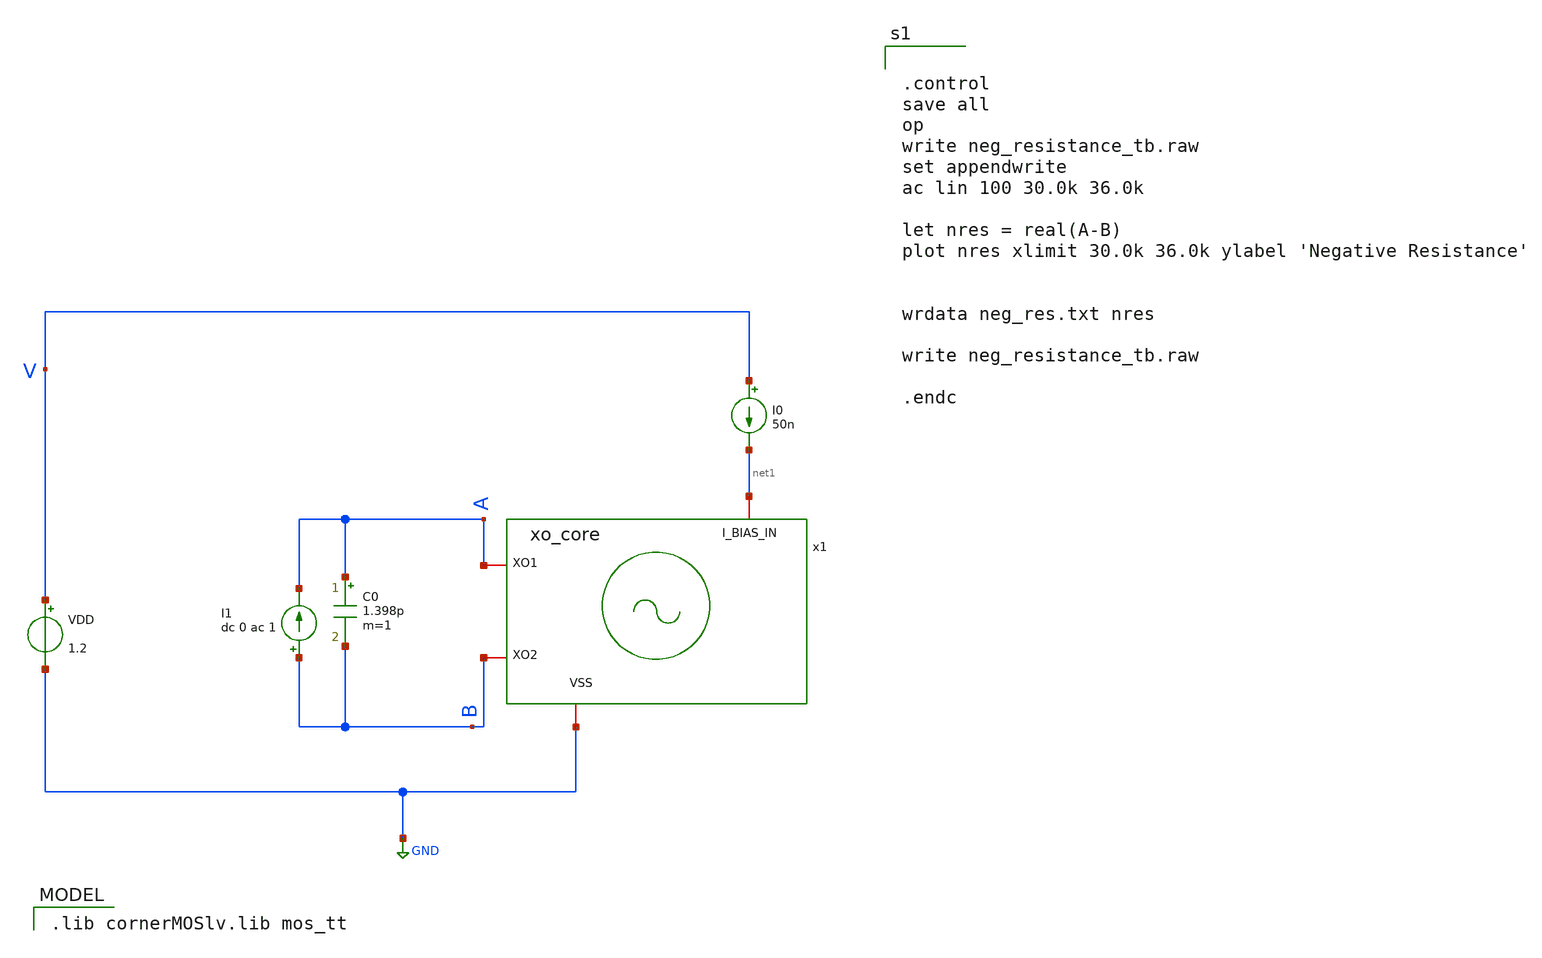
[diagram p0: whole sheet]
** sch_path: neg_resistance_tb.sch
**.subckt neg_resistance_tb
C0 A B 1.398p m=1
I0 V net1 50n
I1 B A dc 0 ac 1
VDD V GND 1.2
x1 net1 B A GND xo_core
**** begin user architecture code


.control
save all
op
write neg_resistance_tb.raw
set appendwrite
ac lin 100 30.0k 36.0k

let nres = real(A-B)
plot nres xlimit 30.0k 36.0k ylabel 'Negative Resistance'


wrdata neg_res.txt nres

write neg_resistance_tb.raw

.endc


 .lib cornerMOSlv.lib mos_tt

**** end user architecture code
**.ends

* expanding   symbol:  xo_core.sym # of pins=4
** sym_path: xo_core.sym
** sch_path: xo_core.sch
.subckt xo_core I_BIAS_IN XO2 XO1 VSS
*.iopin VSS
*.ipin I_BIAS_IN
*.iopin XO1
*.iopin XO2
XM2 net1 XO2 XO2 XO2 sg13_lv_pmos w=0.5u l=2u ng=1 m=1 mm_ok=1
XM3 net1 XO1 XO1 XO1 sg13_lv_pmos w=0.5u l=2u ng=1 m=1 mm_ok=1
XM1 XO2 XO1 VSS VSS sg13_lv_nmos w=2.0u l=0.5u ng=1 m=1 mm_ok=1
C2 XO2 VSS 8p m=1
C1 XO1 VSS 8p m=1
Vmeas I_BIAS_IN XO2 0
.save i(vmeas)
.ends

.GLOBAL GND
.end
